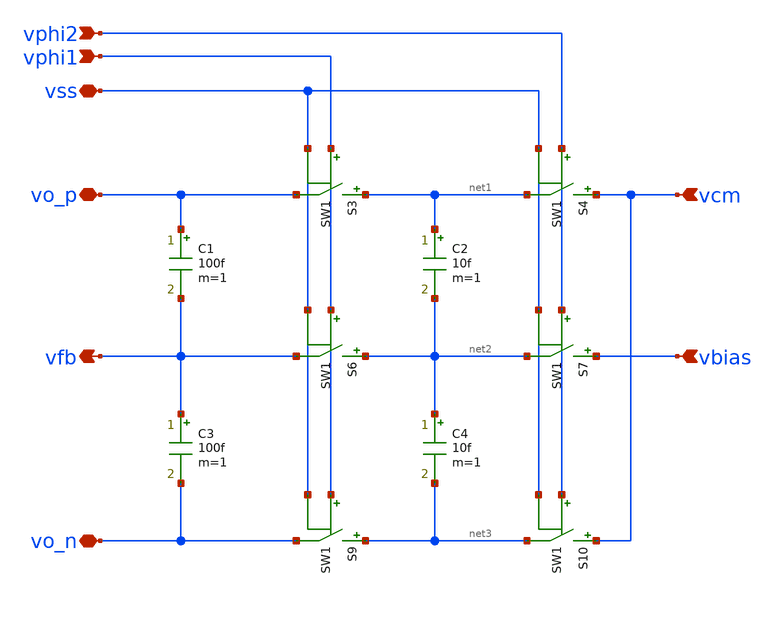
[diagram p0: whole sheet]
** sch_path: xschem/cmfb_sc.sch
**.subckt cmfb_sc vcm vphi2 vphi1 vss vbias vo_p vo_n vfb
*.ipin vcm
*.ipin vphi2
*.ipin vphi1
*.iopin vss
*.ipin vbias
*.iopin vo_p
*.iopin vo_n
*.opin vfb
C1 vo_p vfb 100f m=1
C2 net1 net2 10f m=1
C3 vfb vo_n 100f m=1
C4 net2 net3 10f m=1
S3 net1 vo_p vphi1 vss SW1
S4 vcm net1 vphi2 vss SW1
S6 net2 vfb vphi1 vss SW1
S7 vbias net2 vphi2 vss SW1
S9 net3 vo_n vphi1 vss SW1
S10 vcm net3 vphi2 vss SW1
**.ends
**** begin user architecture code
.MODEL SW1 SW( VT=0.75 VH=0.01 RON=1 ROFF=1G )
**** end user architecture code
.end
